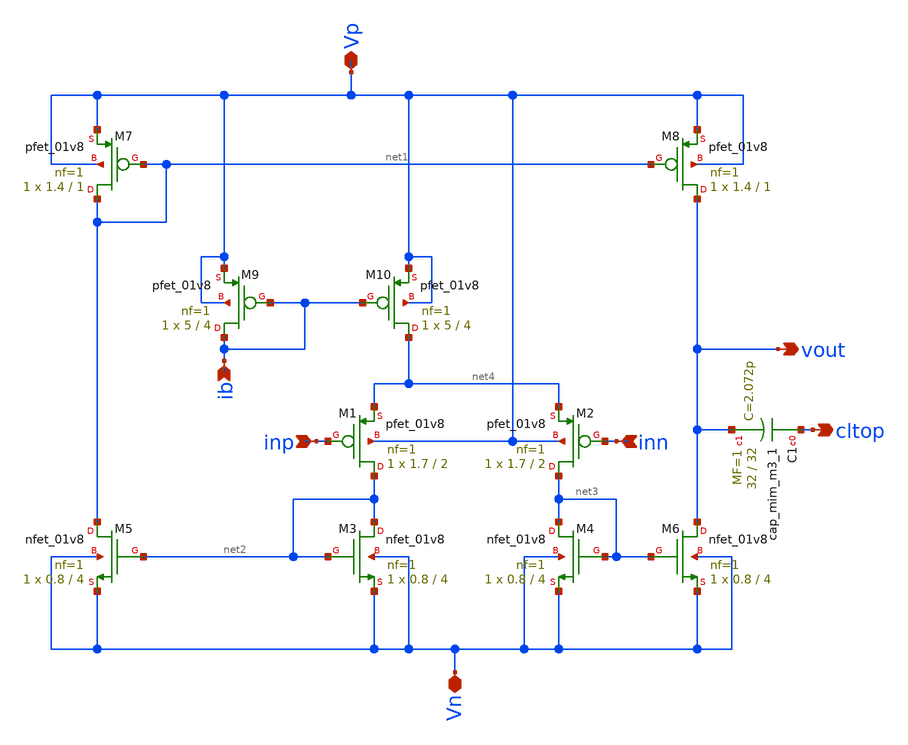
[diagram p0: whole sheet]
** sch_path: xschem/OTA.sch
**.subckt OTA inp inn vout Vp Vn ib cltop
*.ipin inp
*.ipin inn
*.opin vout
*.iopin Vp
*.iopin Vn
*.ipin ib
*.opin cltop
XM7 net1 net1 Vp Vp sky130_fd_pr__pfet_01v8 L=1 W=1.4 nf=1 ad='int((nf+1)/2) * W/nf * 0.29' as='int((nf+2)/2) * W/nf * 0.29'
+ pd='2*int((nf+1)/2) * (W/nf + 0.29)' ps='2*int((nf+2)/2) * (W/nf + 0.29)' nrd='0.29 / W' nrs='0.29 / W'
+ sa=0 sb=0 sd=0 mult=1 m=1
XM8 vout net1 Vp Vp sky130_fd_pr__pfet_01v8 L=1 W=1.4 nf=1 ad='int((nf+1)/2) * W/nf * 0.29' as='int((nf+2)/2) * W/nf * 0.29'
+ pd='2*int((nf+1)/2) * (W/nf + 0.29)' ps='2*int((nf+2)/2) * (W/nf + 0.29)' nrd='0.29 / W' nrs='0.29 / W'
+ sa=0 sb=0 sd=0 mult=1 m=1
XM9 ib ib Vp Vp sky130_fd_pr__pfet_01v8 L=4 W=5 nf=1 ad='int((nf+1)/2) * W/nf * 0.29' as='int((nf+2)/2) * W/nf * 0.29'
+ pd='2*int((nf+1)/2) * (W/nf + 0.29)' ps='2*int((nf+2)/2) * (W/nf + 0.29)' nrd='0.29 / W' nrs='0.29 / W'
+ sa=0 sb=0 sd=0 mult=1 m=1
XM10 net4 ib Vp Vp sky130_fd_pr__pfet_01v8 L=4 W=5 nf=1 ad='int((nf+1)/2) * W/nf * 0.29' as='int((nf+2)/2) * W/nf * 0.29'
+ pd='2*int((nf+1)/2) * (W/nf + 0.29)' ps='2*int((nf+2)/2) * (W/nf + 0.29)' nrd='0.29 / W' nrs='0.29 / W'
+ sa=0 sb=0 sd=0 mult=1 m=1
XM1 net2 inp net4 Vp sky130_fd_pr__pfet_01v8 L=2 W=1.7 nf=1 ad='int((nf+1)/2) * W/nf * 0.29' as='int((nf+2)/2) * W/nf * 0.29'
+ pd='2*int((nf+1)/2) * (W/nf + 0.29)' ps='2*int((nf+2)/2) * (W/nf + 0.29)' nrd='0.29 / W' nrs='0.29 / W'
+ sa=0 sb=0 sd=0 mult=1 m=1
XM2 net3 inn net4 Vp sky130_fd_pr__pfet_01v8 L=2 W=1.7 nf=1 ad='int((nf+1)/2) * W/nf * 0.29' as='int((nf+2)/2) * W/nf * 0.29'
+ pd='2*int((nf+1)/2) * (W/nf + 0.29)' ps='2*int((nf+2)/2) * (W/nf + 0.29)' nrd='0.29 / W' nrs='0.29 / W'
+ sa=0 sb=0 sd=0 mult=1 m=1
XM3 net2 net2 Vn Vn sky130_fd_pr__nfet_01v8 L=4 W=0.8 nf=1 ad='int((nf+1)/2) * W/nf * 0.29' as='int((nf+2)/2) * W/nf * 0.29'
+ pd='2*int((nf+1)/2) * (W/nf + 0.29)' ps='2*int((nf+2)/2) * (W/nf + 0.29)' nrd='0.29 / W' nrs='0.29 / W'
+ sa=0 sb=0 sd=0 mult=1 m=1
XM4 net3 net3 Vn Vn sky130_fd_pr__nfet_01v8 L=4 W=0.8 nf=1 ad='int((nf+1)/2) * W/nf * 0.29' as='int((nf+2)/2) * W/nf * 0.29'
+ pd='2*int((nf+1)/2) * (W/nf + 0.29)' ps='2*int((nf+2)/2) * (W/nf + 0.29)' nrd='0.29 / W' nrs='0.29 / W'
+ sa=0 sb=0 sd=0 mult=1 m=1
XM6 vout net3 Vn Vn sky130_fd_pr__nfet_01v8 L=4 W=0.8 nf=1 ad='int((nf+1)/2) * W/nf * 0.29' as='int((nf+2)/2) * W/nf * 0.29'
+ pd='2*int((nf+1)/2) * (W/nf + 0.29)' ps='2*int((nf+2)/2) * (W/nf + 0.29)' nrd='0.29 / W' nrs='0.29 / W'
+ sa=0 sb=0 sd=0 mult=1 m=1
XM5 net1 net2 Vn Vn sky130_fd_pr__nfet_01v8 L=4 W=0.8 nf=1 ad='int((nf+1)/2) * W/nf * 0.29' as='int((nf+2)/2) * W/nf * 0.29'
+ pd='2*int((nf+1)/2) * (W/nf + 0.29)' ps='2*int((nf+2)/2) * (W/nf + 0.29)' nrd='0.29 / W' nrs='0.29 / W'
+ sa=0 sb=0 sd=0 mult=1 m=1
XC1 cltop vout sky130_fd_pr__cap_mim_m3_1 W=32 L=32 MF=1 m=1
**.ends
.end
